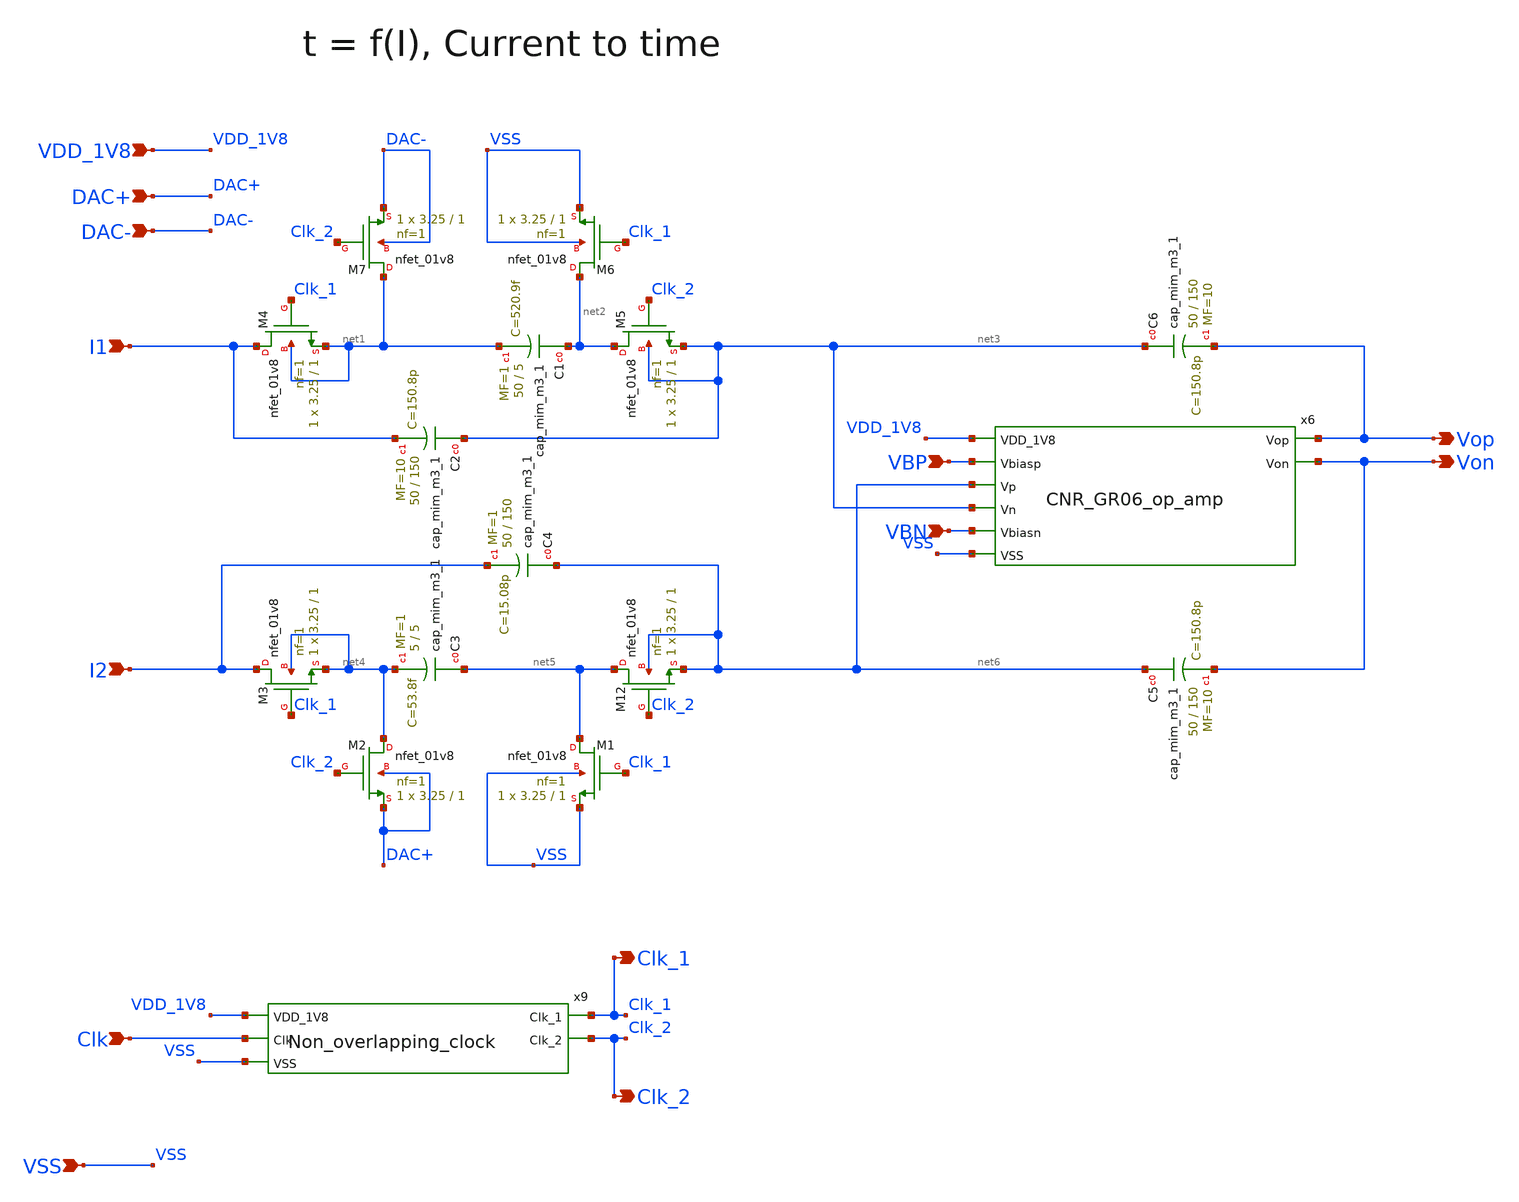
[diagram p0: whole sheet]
** sch_path: design/CNR_GR06_SKY130NM/CNR_GR06_I_to_t.sch
**.subckt CNR_GR06_I_to_t I2 VDD_1V8 VSS I1 Clk Von Vop Clk_1 Clk_2 DAC+ DAC- VBN VBP
*.ipin I2
*.ipin VDD_1V8
*.ipin VSS
*.ipin I1
*.ipin Clk
*.opin Von
*.opin Vop
*.opin Clk_1
*.opin Clk_2
*.ipin DAC+
*.ipin DAC-
*.ipin VBN
*.ipin VBP
XC1 net2 net1 sky130_fd_pr__cap_mim_m3_1 W=50 L=5 MF=1 m=1
XC2 net3 I1 sky130_fd_pr__cap_mim_m3_1 W=50 L=150 MF=10 m=10
XC3 net5 net4 sky130_fd_pr__cap_mim_m3_1 W=5 L=5 MF=1 m=1
XC4 net6 I2 sky130_fd_pr__cap_mim_m3_1 W=50 L=150 MF=1 m=1
XC5 net6 Von sky130_fd_pr__cap_mim_m3_1 W=50 L=150 MF=10 m=10
XC6 net3 Vop sky130_fd_pr__cap_mim_m3_1 W=50 L=150 MF=10 m=10
x9 VDD_1V8 Clk Clk_1 Clk_2 VSS Non_overlapping_clock
XM12 net5 Clk_2 net6 net6 sky130_fd_pr__nfet_01v8 L=1 W=3.25 nf=1 ad='int((nf+1)/2) * W/nf * 0.29' as='int((nf+2)/2) * W/nf * 0.29'
+ pd='2*int((nf+1)/2) * (W/nf + 0.29)' ps='2*int((nf+2)/2) * (W/nf + 0.29)' nrd='0.29 / W' nrs='0.29 / W'
+ sa=0 sb=0 sd=0 mult=1 m=1
XM1 net5 Clk_1 VSS VSS sky130_fd_pr__nfet_01v8 L=1 W=3.25 nf=1 ad='int((nf+1)/2) * W/nf * 0.29' as='int((nf+2)/2) * W/nf * 0.29'
+ pd='2*int((nf+1)/2) * (W/nf + 0.29)' ps='2*int((nf+2)/2) * (W/nf + 0.29)' nrd='0.29 / W' nrs='0.29 / W'
+ sa=0 sb=0 sd=0 mult=1 m=1
XM2 net4 Clk_2 DAC+ DAC+ sky130_fd_pr__nfet_01v8 L=1 W=3.25 nf=1 ad='int((nf+1)/2) * W/nf * 0.29' as='int((nf+2)/2) * W/nf * 0.29'
+ pd='2*int((nf+1)/2) * (W/nf + 0.29)' ps='2*int((nf+2)/2) * (W/nf + 0.29)' nrd='0.29 / W' nrs='0.29 / W'
+ sa=0 sb=0 sd=0 mult=1 m=1
XM3 I2 Clk_1 net4 net4 sky130_fd_pr__nfet_01v8 L=1 W=3.25 nf=1 ad='int((nf+1)/2) * W/nf * 0.29' as='int((nf+2)/2) * W/nf * 0.29'
+ pd='2*int((nf+1)/2) * (W/nf + 0.29)' ps='2*int((nf+2)/2) * (W/nf + 0.29)' nrd='0.29 / W' nrs='0.29 / W'
+ sa=0 sb=0 sd=0 mult=1 m=1
XM4 I1 Clk_1 net1 net1 sky130_fd_pr__nfet_01v8 L=1 W=3.25 nf=1 ad='int((nf+1)/2) * W/nf * 0.29' as='int((nf+2)/2) * W/nf * 0.29'
+ pd='2*int((nf+1)/2) * (W/nf + 0.29)' ps='2*int((nf+2)/2) * (W/nf + 0.29)' nrd='0.29 / W' nrs='0.29 / W'
+ sa=0 sb=0 sd=0 mult=1 m=1
XM5 net2 Clk_2 net3 net3 sky130_fd_pr__nfet_01v8 L=1 W=3.25 nf=1 ad='int((nf+1)/2) * W/nf * 0.29' as='int((nf+2)/2) * W/nf * 0.29'
+ pd='2*int((nf+1)/2) * (W/nf + 0.29)' ps='2*int((nf+2)/2) * (W/nf + 0.29)' nrd='0.29 / W' nrs='0.29 / W'
+ sa=0 sb=0 sd=0 mult=1 m=1
XM6 net2 Clk_1 VSS VSS sky130_fd_pr__nfet_01v8 L=1 W=3.25 nf=1 ad='int((nf+1)/2) * W/nf * 0.29' as='int((nf+2)/2) * W/nf * 0.29'
+ pd='2*int((nf+1)/2) * (W/nf + 0.29)' ps='2*int((nf+2)/2) * (W/nf + 0.29)' nrd='0.29 / W' nrs='0.29 / W'
+ sa=0 sb=0 sd=0 mult=1 m=1
XM7 net1 Clk_2 DAC- DAC- sky130_fd_pr__nfet_01v8 L=1 W=3.25 nf=1 ad='int((nf+1)/2) * W/nf * 0.29' as='int((nf+2)/2) * W/nf * 0.29'
+ pd='2*int((nf+1)/2) * (W/nf + 0.29)' ps='2*int((nf+2)/2) * (W/nf + 0.29)' nrd='0.29 / W' nrs='0.29 / W'
+ sa=0 sb=0 sd=0 mult=1 m=1
x6 VDD_1V8 VBP Vop net6 Von net3 VBN VSS CNR_GR06_op_amp
**.ends
.end
